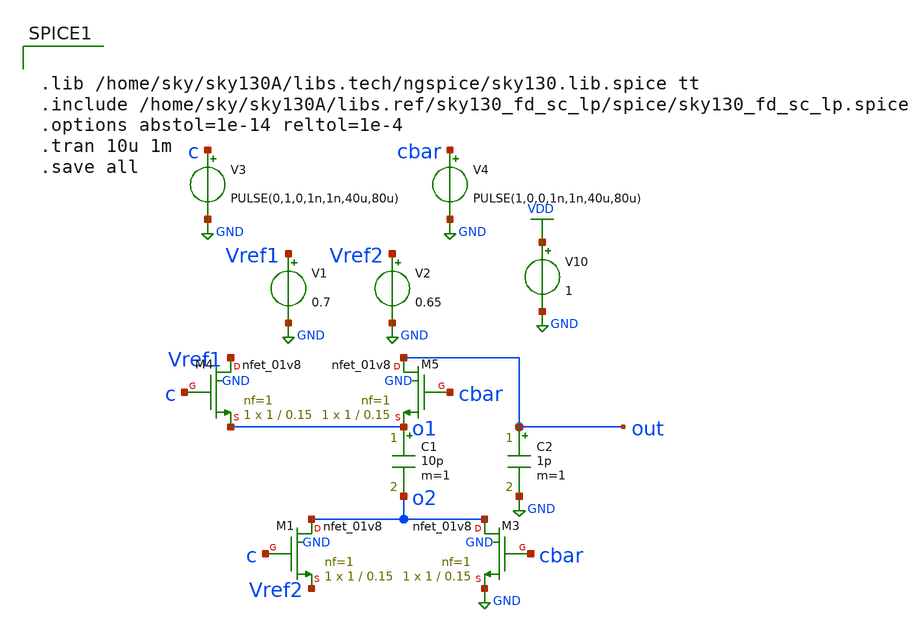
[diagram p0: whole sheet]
** sch_path: xschem/comparator/analogmux_tb.sch
**.subckt analogmux_tb
V10 VDD GND 1
V1 Vref1 GND 0.7
V2 Vref2 GND 0.65
V3 c GND PULSE(0,1,0,1n,1n,40u,80u)
V4 cbar GND PULSE(1,0,0,1n,1n,40u,80u)
C1 o1 o2 10p m=1
C2 out GND 1p m=1
XM1 o2 c Vref2 GND sky130_fd_pr__nfet_01v8 L=0.15 W=1 nf=1 ad='int((nf+1)/2) * W/nf * 0.29' as='int((nf+2)/2) * W/nf * 0.29'
+ pd='2*int((nf+1)/2) * (W/nf + 0.29)' ps='2*int((nf+2)/2) * (W/nf + 0.29)' nrd='0.29 / W' nrs='0.29 / W'
+ sa=0 sb=0 sd=0 mult=1 m=1
XM3 o2 cbar GND GND sky130_fd_pr__nfet_01v8 L=0.15 W=1 nf=1 ad='int((nf+1)/2) * W/nf * 0.29' as='int((nf+2)/2) * W/nf * 0.29'
+ pd='2*int((nf+1)/2) * (W/nf + 0.29)' ps='2*int((nf+2)/2) * (W/nf + 0.29)' nrd='0.29 / W' nrs='0.29 / W'
+ sa=0 sb=0 sd=0 mult=1 m=1
XM4 Vref1 c o1 GND sky130_fd_pr__nfet_01v8 L=0.15 W=1 nf=1 ad='int((nf+1)/2) * W/nf * 0.29' as='int((nf+2)/2) * W/nf * 0.29'
+ pd='2*int((nf+1)/2) * (W/nf + 0.29)' ps='2*int((nf+2)/2) * (W/nf + 0.29)' nrd='0.29 / W' nrs='0.29 / W'
+ sa=0 sb=0 sd=0 mult=1 m=1
XM5 out cbar o1 GND sky130_fd_pr__nfet_01v8 L=0.15 W=1 nf=1 ad='int((nf+1)/2) * W/nf * 0.29' as='int((nf+2)/2) * W/nf * 0.29'
+ pd='2*int((nf+1)/2) * (W/nf + 0.29)' ps='2*int((nf+2)/2) * (W/nf + 0.29)' nrd='0.29 / W' nrs='0.29 / W'
+ sa=0 sb=0 sd=0 mult=1 m=1
**** begin user architecture code


.lib /home/sky/sky130A/libs.tech/ngspice/sky130.lib.spice tt
.include /home/sky/sky130A/libs.ref/sky130_fd_sc_lp/spice/sky130_fd_sc_lp.spice
.options abstol=1e-14 reltol=1e-4
.tran 10u 1m
.save all


**** end user architecture code
**.ends
.GLOBAL VDD
.GLOBAL GND
.end
